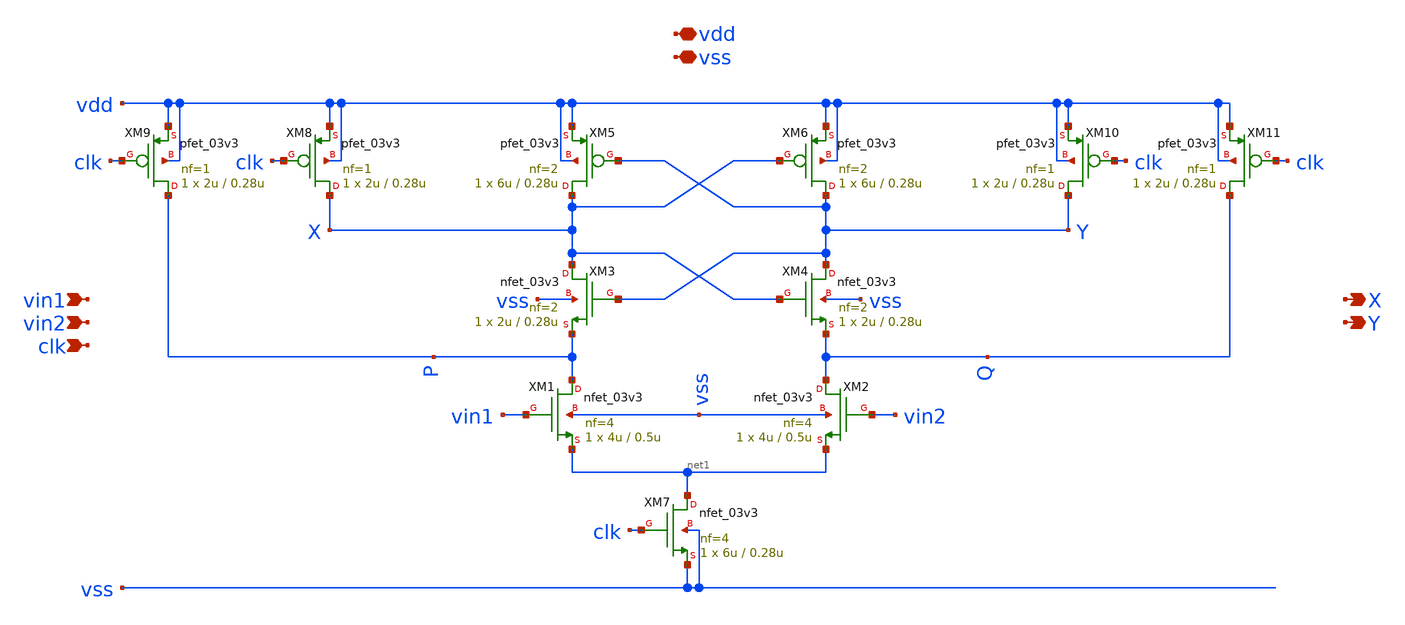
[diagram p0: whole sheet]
** sch_path: designs/libs/core_analog/saradc/comparator.sch
**.subckt comparator vdd vss vin1 vin2 clk X Y
*.iopin vdd
*.iopin vss
*.ipin vin1
*.ipin vin2
*.ipin clk
*.opin X
*.opin Y
XM1 P vin1 net1 vss nfet_03v3 L=0.5u W=4u nf=4 ad='int((nf+1)/2) * W/nf * 0.18u' as='int((nf+2)/2) * W/nf * 0.18u'
+ pd='2*int((nf+1)/2) * (W/nf + 0.18u)' ps='2*int((nf+2)/2) * (W/nf + 0.18u)' nrd='0.18u / W' nrs='0.18u / W'
+ sa=0 sb=0 sd=0 m=1
XM2 Q vin2 net1 vss nfet_03v3 L=0.5u W=4u nf=4 ad='int((nf+1)/2) * W/nf * 0.18u' as='int((nf+2)/2) * W/nf * 0.18u'
+ pd='2*int((nf+1)/2) * (W/nf + 0.18u)' ps='2*int((nf+2)/2) * (W/nf + 0.18u)' nrd='0.18u / W' nrs='0.18u / W'
+ sa=0 sb=0 sd=0 m=1
XM3 X Y P vss nfet_03v3 L=0.28u W=2u nf=2 ad='int((nf+1)/2) * W/nf * 0.18u' as='int((nf+2)/2) * W/nf * 0.18u'
+ pd='2*int((nf+1)/2) * (W/nf + 0.18u)' ps='2*int((nf+2)/2) * (W/nf + 0.18u)' nrd='0.18u / W' nrs='0.18u / W'
+ sa=0 sb=0 sd=0 m=1
XM4 Y X Q vss nfet_03v3 L=0.28u W=2u nf=2 ad='int((nf+1)/2) * W/nf * 0.18u' as='int((nf+2)/2) * W/nf * 0.18u'
+ pd='2*int((nf+1)/2) * (W/nf + 0.18u)' ps='2*int((nf+2)/2) * (W/nf + 0.18u)' nrd='0.18u / W' nrs='0.18u / W'
+ sa=0 sb=0 sd=0 m=1
XM5 X Y vdd vdd pfet_03v3 L=0.28u W=6u nf=2 ad='int((nf+1)/2) * W/nf * 0.18u' as='int((nf+2)/2) * W/nf * 0.18u'
+ pd='2*int((nf+1)/2) * (W/nf + 0.18u)' ps='2*int((nf+2)/2) * (W/nf + 0.18u)' nrd='0.18u / W' nrs='0.18u / W'
+ sa=0 sb=0 sd=0 m=1
XM6 Y X vdd vdd pfet_03v3 L=0.28u W=6u nf=2 ad='int((nf+1)/2) * W/nf * 0.18u' as='int((nf+2)/2) * W/nf * 0.18u'
+ pd='2*int((nf+1)/2) * (W/nf + 0.18u)' ps='2*int((nf+2)/2) * (W/nf + 0.18u)' nrd='0.18u / W' nrs='0.18u / W'
+ sa=0 sb=0 sd=0 m=1
XM7 net1 clk vss vss nfet_03v3 L=0.28u W=6u nf=4 ad='int((nf+1)/2) * W/nf * 0.18u' as='int((nf+2)/2) * W/nf * 0.18u'
+ pd='2*int((nf+1)/2) * (W/nf + 0.18u)' ps='2*int((nf+2)/2) * (W/nf + 0.18u)' nrd='0.18u / W' nrs='0.18u / W'
+ sa=0 sb=0 sd=0 m=1
XM8 X clk vdd vdd pfet_03v3 L=0.28u W=2u nf=1 ad='int((nf+1)/2) * W/nf * 0.18u' as='int((nf+2)/2) * W/nf * 0.18u'
+ pd='2*int((nf+1)/2) * (W/nf + 0.18u)' ps='2*int((nf+2)/2) * (W/nf + 0.18u)' nrd='0.18u / W' nrs='0.18u / W'
+ sa=0 sb=0 sd=0 m=1
XM9 P clk vdd vdd pfet_03v3 L=0.28u W=2u nf=1 ad='int((nf+1)/2) * W/nf * 0.18u' as='int((nf+2)/2) * W/nf * 0.18u'
+ pd='2*int((nf+1)/2) * (W/nf + 0.18u)' ps='2*int((nf+2)/2) * (W/nf + 0.18u)' nrd='0.18u / W' nrs='0.18u / W'
+ sa=0 sb=0 sd=0 m=1
XM10 Y clk vdd vdd pfet_03v3 L=0.28u W=2u nf=1 ad='int((nf+1)/2) * W/nf * 0.18u' as='int((nf+2)/2) * W/nf * 0.18u'
+ pd='2*int((nf+1)/2) * (W/nf + 0.18u)' ps='2*int((nf+2)/2) * (W/nf + 0.18u)' nrd='0.18u / W' nrs='0.18u / W'
+ sa=0 sb=0 sd=0 m=1
XM11 Q clk vdd vdd pfet_03v3 L=0.28u W=2u nf=1 ad='int((nf+1)/2) * W/nf * 0.18u' as='int((nf+2)/2) * W/nf * 0.18u'
+ pd='2*int((nf+1)/2) * (W/nf + 0.18u)' ps='2*int((nf+2)/2) * (W/nf + 0.18u)' nrd='0.18u / W' nrs='0.18u / W'
+ sa=0 sb=0 sd=0 m=1
**.ends
.end
